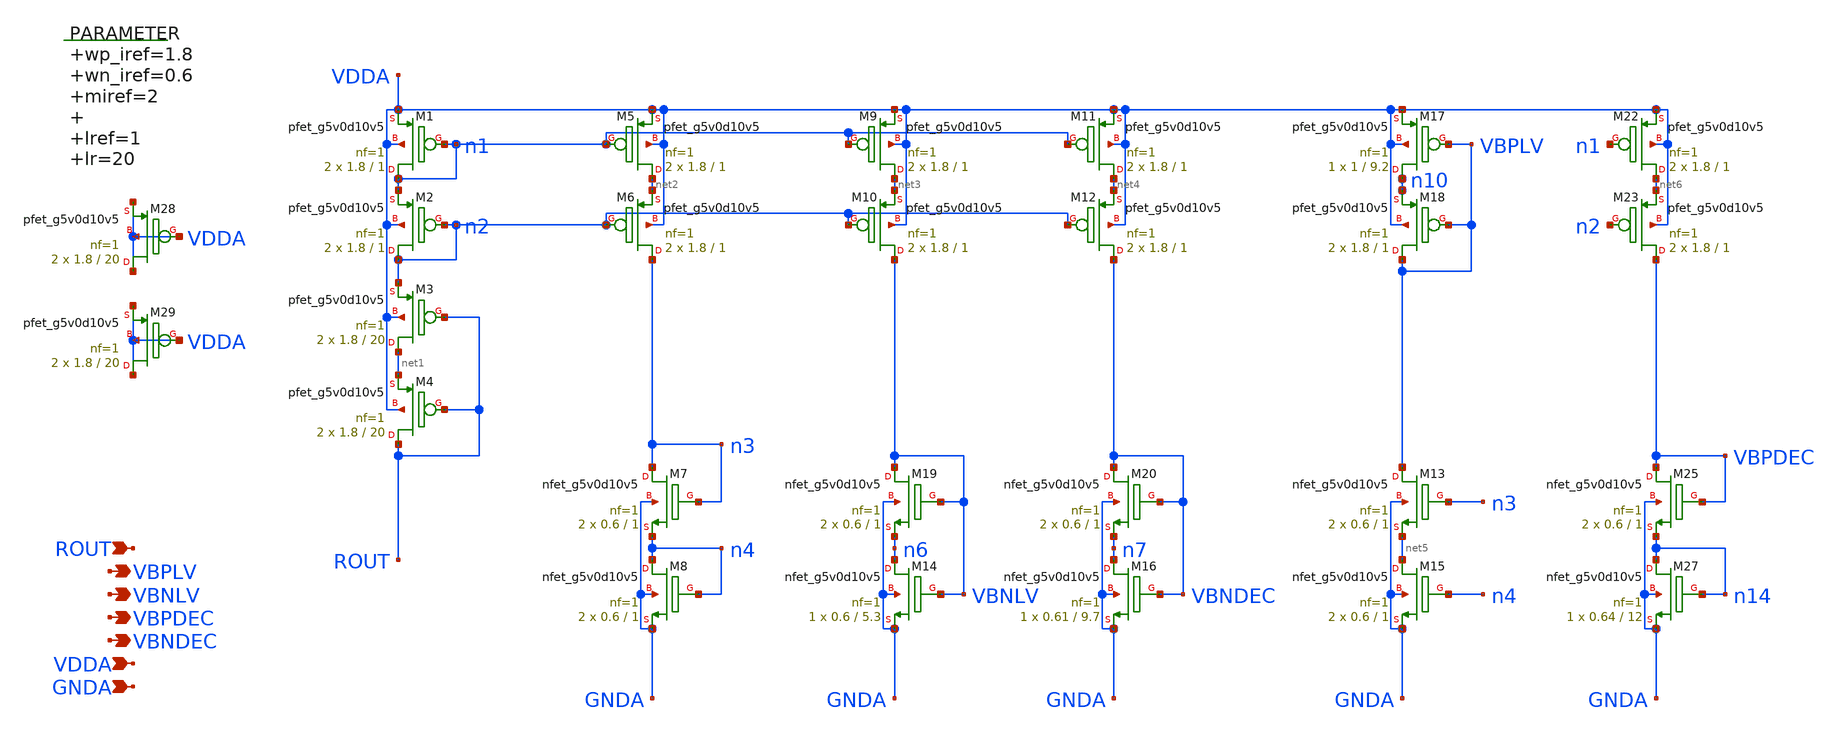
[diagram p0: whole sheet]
** sch_path: xschem/bias_lvsf.sch
**.subckt bias_lvsf ROUT VBPLV VBNLV VBPDEC VBNDEC VDDA GNDA
*.ipin ROUT
*.opin VBPLV
*.opin VBNLV
*.opin VBPDEC
*.opin VBNDEC
*.ipin VDDA
*.ipin GNDA
.param wp_iref=1.8 wn_iref=0.6 miref=2 lref=1 lr=20
XM1 n1 n1 VDDA VDDA sky130_fd_pr__pfet_g5v0d10v5 L=1 W=1.8 nf=1 ad='int((nf+1)/2) * W/nf * 0.29' as='int((nf+2)/2) * W/nf * 0.29'
+ pd='2*int((nf+1)/2) * (W/nf + 0.29)' ps='2*int((nf+2)/2) * (W/nf + 0.29)' nrd='0.29 / W' nrs='0.29 / W'
+ sa=0 sb=0 sd=0 mult=2 m=2
XM2 n2 n2 n1 VDDA sky130_fd_pr__pfet_g5v0d10v5 L=1 W=1.8 nf=1 ad='int((nf+1)/2) * W/nf * 0.29' as='int((nf+2)/2) * W/nf * 0.29'
+ pd='2*int((nf+1)/2) * (W/nf + 0.29)' ps='2*int((nf+2)/2) * (W/nf + 0.29)' nrd='0.29 / W' nrs='0.29 / W'
+ sa=0 sb=0 sd=0 mult=2 m=2
XM3 net1 ROUT n2 VDDA sky130_fd_pr__pfet_g5v0d10v5 L=20 W=1.8 nf=1 ad='int((nf+1)/2) * W/nf * 0.29' as='int((nf+2)/2) * W/nf * 0.29'
+ pd='2*int((nf+1)/2) * (W/nf + 0.29)' ps='2*int((nf+2)/2) * (W/nf + 0.29)' nrd='0.29 / W' nrs='0.29 / W'
+ sa=0 sb=0 sd=0 mult=2 m=2
XM4 ROUT ROUT net1 VDDA sky130_fd_pr__pfet_g5v0d10v5 L=20 W=1.8 nf=1 ad='int((nf+1)/2) * W/nf * 0.29'
+ as='int((nf+2)/2) * W/nf * 0.29' pd='2*int((nf+1)/2) * (W/nf + 0.29)' ps='2*int((nf+2)/2) * (W/nf + 0.29)'
+ nrd='0.29 / W' nrs='0.29 / W' sa=0 sb=0 sd=0 mult=2 m=2
XM5 net2 n1 VDDA VDDA sky130_fd_pr__pfet_g5v0d10v5 L=1 W=1.8 nf=1 ad='int((nf+1)/2) * W/nf * 0.29' as='int((nf+2)/2) * W/nf * 0.29'
+ pd='2*int((nf+1)/2) * (W/nf + 0.29)' ps='2*int((nf+2)/2) * (W/nf + 0.29)' nrd='0.29 / W' nrs='0.29 / W'
+ sa=0 sb=0 sd=0 mult=2 m=2
XM6 n3 n2 net2 VDDA sky130_fd_pr__pfet_g5v0d10v5 L=1 W=1.8 nf=1 ad='int((nf+1)/2) * W/nf * 0.29' as='int((nf+2)/2) * W/nf * 0.29'
+ pd='2*int((nf+1)/2) * (W/nf + 0.29)' ps='2*int((nf+2)/2) * (W/nf + 0.29)' nrd='0.29 / W' nrs='0.29 / W'
+ sa=0 sb=0 sd=0 mult=2 m=2
XM9 net3 n1 VDDA VDDA sky130_fd_pr__pfet_g5v0d10v5 L=1 W=1.8 nf=1 ad='int((nf+1)/2) * W/nf * 0.29' as='int((nf+2)/2) * W/nf * 0.29'
+ pd='2*int((nf+1)/2) * (W/nf + 0.29)' ps='2*int((nf+2)/2) * (W/nf + 0.29)' nrd='0.29 / W' nrs='0.29 / W'
+ sa=0 sb=0 sd=0 mult=2 m=2
XM10 VBNLV n2 net3 VDDA sky130_fd_pr__pfet_g5v0d10v5 L=1 W=1.8 nf=1 ad='int((nf+1)/2) * W/nf * 0.29'
+ as='int((nf+2)/2) * W/nf * 0.29' pd='2*int((nf+1)/2) * (W/nf + 0.29)' ps='2*int((nf+2)/2) * (W/nf + 0.29)'
+ nrd='0.29 / W' nrs='0.29 / W' sa=0 sb=0 sd=0 mult=2 m=2
XM11 net4 n1 VDDA VDDA sky130_fd_pr__pfet_g5v0d10v5 L=1 W=1.8 nf=1 ad='int((nf+1)/2) * W/nf * 0.29' as='int((nf+2)/2) * W/nf * 0.29'
+ pd='2*int((nf+1)/2) * (W/nf + 0.29)' ps='2*int((nf+2)/2) * (W/nf + 0.29)' nrd='0.29 / W' nrs='0.29 / W'
+ sa=0 sb=0 sd=0 mult=2 m=2
XM12 VBNDEC n2 net4 VDDA sky130_fd_pr__pfet_g5v0d10v5 L=1 W=1.8 nf=1 ad='int((nf+1)/2) * W/nf * 0.29'
+ as='int((nf+2)/2) * W/nf * 0.29' pd='2*int((nf+1)/2) * (W/nf + 0.29)' ps='2*int((nf+2)/2) * (W/nf + 0.29)'
+ nrd='0.29 / W' nrs='0.29 / W' sa=0 sb=0 sd=0 mult=2 m=2
XM22 net6 n1 VDDA VDDA sky130_fd_pr__pfet_g5v0d10v5 L=1 W=1.8 nf=1 ad='int((nf+1)/2) * W/nf * 0.29' as='int((nf+2)/2) * W/nf * 0.29'
+ pd='2*int((nf+1)/2) * (W/nf + 0.29)' ps='2*int((nf+2)/2) * (W/nf + 0.29)' nrd='0.29 / W' nrs='0.29 / W'
+ sa=0 sb=0 sd=0 mult=2 m=2
XM23 VBPDEC n2 net6 VDDA sky130_fd_pr__pfet_g5v0d10v5 L=1 W=1.8 nf=1 ad='int((nf+1)/2) * W/nf * 0.29'
+ as='int((nf+2)/2) * W/nf * 0.29' pd='2*int((nf+1)/2) * (W/nf + 0.29)' ps='2*int((nf+2)/2) * (W/nf + 0.29)'
+ nrd='0.29 / W' nrs='0.29 / W' sa=0 sb=0 sd=0 mult=2 m=2
XM7 n3 n3 n4 GNDA sky130_fd_pr__nfet_g5v0d10v5 L=1 W=0.6 nf=1 ad='int((nf+1)/2) * W/nf * 0.29' as='int((nf+2)/2) * W/nf * 0.29'
+ pd='2*int((nf+1)/2) * (W/nf + 0.29)' ps='2*int((nf+2)/2) * (W/nf + 0.29)' nrd='0.29 / W' nrs='0.29 / W'
+ sa=0 sb=0 sd=0 mult=2 m=2
XM8 n4 n4 GNDA GNDA sky130_fd_pr__nfet_g5v0d10v5 L=1 W=0.6 nf=1 ad='int((nf+1)/2) * W/nf * 0.29' as='int((nf+2)/2) * W/nf * 0.29'
+ pd='2*int((nf+1)/2) * (W/nf + 0.29)' ps='2*int((nf+2)/2) * (W/nf + 0.29)' nrd='0.29 / W' nrs='0.29 / W'
+ sa=0 sb=0 sd=0 mult=2 m=2
XM13 VBPLV n3 net5 GNDA sky130_fd_pr__nfet_g5v0d10v5 L=1 W=0.6 nf=1 ad='int((nf+1)/2) * W/nf * 0.29'
+ as='int((nf+2)/2) * W/nf * 0.29' pd='2*int((nf+1)/2) * (W/nf + 0.29)' ps='2*int((nf+2)/2) * (W/nf + 0.29)'
+ nrd='0.29 / W' nrs='0.29 / W' sa=0 sb=0 sd=0 mult=2 m=2
XM15 net5 n4 GNDA GNDA sky130_fd_pr__nfet_g5v0d10v5 L=1 W=0.6 nf=1 ad='int((nf+1)/2) * W/nf * 0.29' as='int((nf+2)/2) * W/nf * 0.29'
+ pd='2*int((nf+1)/2) * (W/nf + 0.29)' ps='2*int((nf+2)/2) * (W/nf + 0.29)' nrd='0.29 / W' nrs='0.29 / W'
+ sa=0 sb=0 sd=0 mult=2 m=2
XM19 VBNLV VBNLV n6 GNDA sky130_fd_pr__nfet_g5v0d10v5 L=1 W=0.6 nf=1 ad='int((nf+1)/2) * W/nf * 0.29'
+ as='int((nf+2)/2) * W/nf * 0.29' pd='2*int((nf+1)/2) * (W/nf + 0.29)' ps='2*int((nf+2)/2) * (W/nf + 0.29)'
+ nrd='0.29 / W' nrs='0.29 / W' sa=0 sb=0 sd=0 mult=2 m=2
XM20 VBNDEC VBNDEC n7 GNDA sky130_fd_pr__nfet_g5v0d10v5 L=1 W=0.6 nf=1 ad='int((nf+1)/2) * W/nf * 0.29'
+ as='int((nf+2)/2) * W/nf * 0.29' pd='2*int((nf+1)/2) * (W/nf + 0.29)' ps='2*int((nf+2)/2) * (W/nf + 0.29)'
+ nrd='0.29 / W' nrs='0.29 / W' sa=0 sb=0 sd=0 mult=2 m=2
XM25 VBPDEC VBPDEC n14 GNDA sky130_fd_pr__nfet_g5v0d10v5 L=1 W=0.6 nf=1 ad='int((nf+1)/2) * W/nf * 0.29'
+ as='int((nf+2)/2) * W/nf * 0.29' pd='2*int((nf+1)/2) * (W/nf + 0.29)' ps='2*int((nf+2)/2) * (W/nf + 0.29)'
+ nrd='0.29 / W' nrs='0.29 / W' sa=0 sb=0 sd=0 mult=2 m=2
XM14 n6 VBNLV GNDA GNDA sky130_fd_pr__nfet_g5v0d10v5 L=5.3 W=0.6 nf=1 ad='int((nf+1)/2) * W/nf * 0.29'
+ as='int((nf+2)/2) * W/nf * 0.29' pd='2*int((nf+1)/2) * (W/nf + 0.29)' ps='2*int((nf+2)/2) * (W/nf + 0.29)'
+ nrd='0.29 / W' nrs='0.29 / W' sa=0 sb=0 sd=0 mult=1 m=1
XM16 n7 VBNDEC GNDA GNDA sky130_fd_pr__nfet_g5v0d10v5 L=9.7 W=0.61 nf=1 ad='int((nf+1)/2) * W/nf * 0.29'
+ as='int((nf+2)/2) * W/nf * 0.29' pd='2*int((nf+1)/2) * (W/nf + 0.29)' ps='2*int((nf+2)/2) * (W/nf + 0.29)'
+ nrd='0.29 / W' nrs='0.29 / W' sa=0 sb=0 sd=0 mult=1 m=1
XM27 n14 n14 GNDA GNDA sky130_fd_pr__nfet_g5v0d10v5 L=12 W=0.64 nf=1 ad='int((nf+1)/2) * W/nf * 0.29'
+ as='int((nf+2)/2) * W/nf * 0.29' pd='2*int((nf+1)/2) * (W/nf + 0.29)' ps='2*int((nf+2)/2) * (W/nf + 0.29)'
+ nrd='0.29 / W' nrs='0.29 / W' sa=0 sb=0 sd=0 mult=1 m=1
XM18 VBPLV VBPLV n10 VDDA sky130_fd_pr__pfet_g5v0d10v5 L=1 W=1.8 nf=1 ad='int((nf+1)/2) * W/nf * 0.29'
+ as='int((nf+2)/2) * W/nf * 0.29' pd='2*int((nf+1)/2) * (W/nf + 0.29)' ps='2*int((nf+2)/2) * (W/nf + 0.29)'
+ nrd='0.29 / W' nrs='0.29 / W' sa=0 sb=0 sd=0 mult=2 m=2
XM17 n10 VBPLV VDDA VDDA sky130_fd_pr__pfet_g5v0d10v5 L=9.2 W=1 nf=1 ad='int((nf+1)/2) * W/nf * 0.29'
+ as='int((nf+2)/2) * W/nf * 0.29' pd='2*int((nf+1)/2) * (W/nf + 0.29)' ps='2*int((nf+2)/2) * (W/nf + 0.29)'
+ nrd='0.29 / W' nrs='0.29 / W' sa=0 sb=0 sd=0 mult=1 m=1
XM28 VDDA VDDA VDDA VDDA sky130_fd_pr__pfet_g5v0d10v5 L=20 W=1.8 nf=1 ad='int((nf+1)/2) * W/nf * 0.29'
+ as='int((nf+2)/2) * W/nf * 0.29' pd='2*int((nf+1)/2) * (W/nf + 0.29)' ps='2*int((nf+2)/2) * (W/nf + 0.29)'
+ nrd='0.29 / W' nrs='0.29 / W' sa=0 sb=0 sd=0 mult=2 m=2
XM29 VDDA VDDA VDDA VDDA sky130_fd_pr__pfet_g5v0d10v5 L=20 W=1.8 nf=1 ad='int((nf+1)/2) * W/nf * 0.29'
+ as='int((nf+2)/2) * W/nf * 0.29' pd='2*int((nf+1)/2) * (W/nf + 0.29)' ps='2*int((nf+2)/2) * (W/nf + 0.29)'
+ nrd='0.29 / W' nrs='0.29 / W' sa=0 sb=0 sd=0 mult=2 m=2
**.ends
.end
